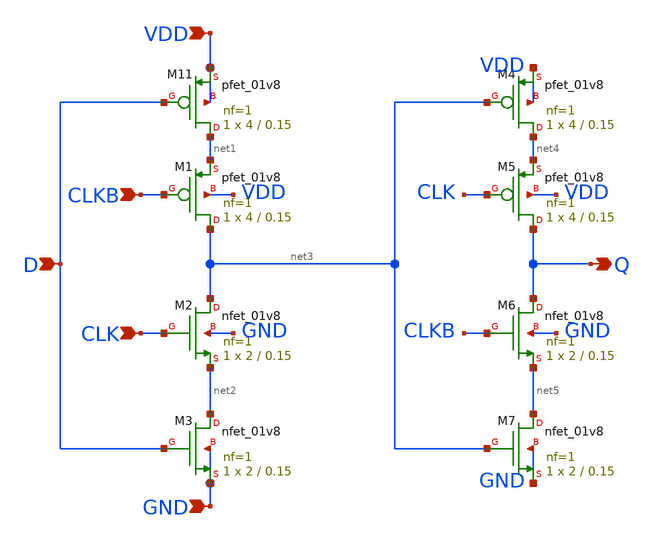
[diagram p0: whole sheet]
** sch_path: pll/dividers_lib/divider_design_trials/Testbench for testing latches/CMOS_d_latch.sch
**.subckt CMOS_d_latch VDD D CLK GND CLKB Q
*.ipin VDD
*.ipin D
*.ipin CLK
*.ipin GND
*.ipin CLKB
*.opin Q
XM11 net1 D VDD VDD sky130_fd_pr__pfet_01v8 L=0.15 W=4 nf=1 ad='int((nf+1)/2) * W/nf * 0.29' as='int((nf+2)/2) * W/nf * 0.29'
+ pd='2*int((nf+1)/2) * (W/nf + 0.29)' ps='2*int((nf+2)/2) * (W/nf + 0.29)' nrd='0.29 / W' nrs='0.29 / W'
+ sa=0 sb=0 sd=0 mult=1 m=1
XM1 net3 CLKB net1 VDD sky130_fd_pr__pfet_01v8 L=0.15 W=4 nf=1 ad='int((nf+1)/2) * W/nf * 0.29' as='int((nf+2)/2) * W/nf * 0.29'
+ pd='2*int((nf+1)/2) * (W/nf + 0.29)' ps='2*int((nf+2)/2) * (W/nf + 0.29)' nrd='0.29 / W' nrs='0.29 / W'
+ sa=0 sb=0 sd=0 mult=1 m=1
XM2 net3 CLK net2 GND sky130_fd_pr__nfet_01v8 L=0.15 W=2 nf=1 ad='int((1 + 1)/2) * 2 / 1 * 0.29' as='int((1 + 2)/2) * 2 / 1 * 0.29'
+ pd='2*int((1 + 1)/2) * (2 / 1 + 0.29)' ps='2*int((1 + 2)/2) * (2 / 1 + 0.29)' nrd='0.29 / 2 ' nrs='0.29 / 2 '
+ sa=0 sb=0 sd=0 mult=1 m=1
XM3 net2 D GND GND sky130_fd_pr__nfet_01v8 L=0.15 W=2 nf=1 ad='int((1 + 1)/2) * 2 / 1 * 0.29' as='int((1 + 2)/2) * 2 / 1 * 0.29'
+ pd='2*int((1 + 1)/2) * (2 / 1 + 0.29)' ps='2*int((1 + 2)/2) * (2 / 1 + 0.29)' nrd='0.29 / 2 ' nrs='0.29 / 2 '
+ sa=0 sb=0 sd=0 mult=1 m=1
XM4 net4 net3 VDD VDD sky130_fd_pr__pfet_01v8 L=0.15 W=4 nf=1 ad='int((nf+1)/2) * W/nf * 0.29' as='int((nf+2)/2) * W/nf * 0.29'
+ pd='2*int((nf+1)/2) * (W/nf + 0.29)' ps='2*int((nf+2)/2) * (W/nf + 0.29)' nrd='0.29 / W' nrs='0.29 / W'
+ sa=0 sb=0 sd=0 mult=1 m=1
XM5 Q CLK net4 VDD sky130_fd_pr__pfet_01v8 L=0.15 W=4 nf=1 ad='int((nf+1)/2) * W/nf * 0.29' as='int((nf+2)/2) * W/nf * 0.29'
+ pd='2*int((nf+1)/2) * (W/nf + 0.29)' ps='2*int((nf+2)/2) * (W/nf + 0.29)' nrd='0.29 / W' nrs='0.29 / W'
+ sa=0 sb=0 sd=0 mult=1 m=1
XM6 Q CLKB net5 GND sky130_fd_pr__nfet_01v8 L=0.15 W=2 nf=1 ad='int((1 + 1)/2) * 2 / 1 * 0.29' as='int((1 + 2)/2) * 2 / 1 * 0.29'
+ pd='2*int((1 + 1)/2) * (2 / 1 + 0.29)' ps='2*int((1 + 2)/2) * (2 / 1 + 0.29)' nrd='0.29 / 2 ' nrs='0.29 / 2 '
+ sa=0 sb=0 sd=0 mult=1 m=1
XM7 net5 net3 GND GND sky130_fd_pr__nfet_01v8 L=0.15 W=2 nf=1 ad='int((1 + 1)/2) * 2 / 1 * 0.29' as='int((1 + 2)/2) * 2 / 1 * 0.29'
+ pd='2*int((1 + 1)/2) * (2 / 1 + 0.29)' ps='2*int((1 + 2)/2) * (2 / 1 + 0.29)' nrd='0.29 / 2 ' nrs='0.29 / 2 '
+ sa=0 sb=0 sd=0 mult=1 m=1
**.ends
.end
